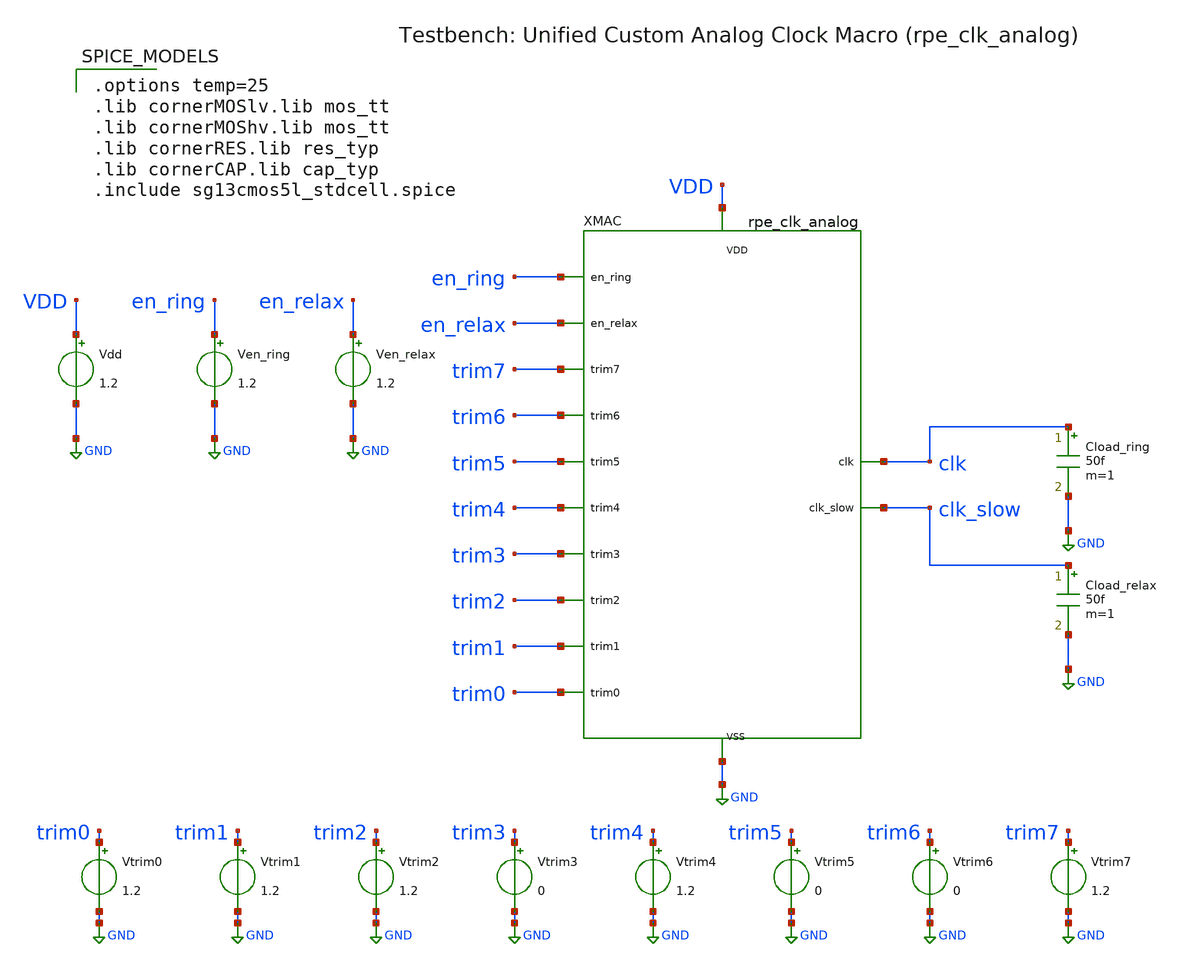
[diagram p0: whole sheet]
** sch_path: analog/clk_macro/tb_rpe_clk_analog.sch
**.subckt tb_rpe_clk_analog
XMAC VDD GND en_ring en_relax trim7 trim6 trim5 trim4 trim3 trim2 trim1 trim0 clk clk_slow
+ rpe_clk_analog
Vdd VDD GND 1.2
Ven_ring en_ring GND 1.2
Ven_relax en_relax GND 1.2
Vtrim0 trim0 GND 1.2
Vtrim1 trim1 GND 1.2
Vtrim2 trim2 GND 1.2
Vtrim3 trim3 GND 0
Vtrim4 trim4 GND 1.2
Vtrim5 trim5 GND 0
Vtrim6 trim6 GND 0
Vtrim7 trim7 GND 1.2
Cload_ring clk GND 50f m=1
Cload_relax clk_slow GND 50f m=1
**** begin user architecture code

.options temp=25
.lib cornerMOSlv.lib mos_tt
.lib cornerMOShv.lib mos_tt
.lib cornerRES.lib res_typ
.lib cornerCAP.lib cap_typ
.include sg13cmos5l_stdcell.spice


**** end user architecture code
**.ends

* expanding   symbol:  clk_macro/rpe_clk_analog.sym # of pins=14
** sym_path: analog/clk_macro/rpe_clk_analog.sym
** sch_path: analog/clk_macro/rpe_clk_analog.sch
.subckt rpe_clk_analog VDD VSS en_ring en_relax trim7 trim6 trim5 trim4 trim3 trim2 trim1 trim0 clk
+ clk_slow
*.iopin VDD
*.iopin VSS
*.ipin en_ring
*.ipin en_relax
*.ipin trim7
*.ipin trim6
*.ipin trim5
*.ipin trim4
*.ipin trim3
*.ipin trim2
*.ipin trim1
*.ipin trim0
*.opin clk
*.opin clk_slow
XEN_NOR net1 en_ring en_relax VDD VSS sg13cmos5l_nor2_1
XEN_OR en_bias net1 VDD VSS sg13cmos5l_inv_1
XBIAS VDD VSS en_bias vpbias vnbias net2 bias
* noconn #net2
XIDAC VDD VSS en_ring vnbias trim7 trim6 trim5 trim4 trim3 trim2 trim1 trim0 ictrl idac_8b
XCCO VDD VSS en_ring ictrl clk cco_core
XRELAX VDD VSS en_relax vpbias vnbias clk_slow relax_core
.ends


* expanding   symbol:  bias/bias.sym # of pins=6
** sym_path: analog/bias/bias.sym
** sch_path: analog/bias/bias.sch
.subckt bias VDD VSS en vpbias vnbias ibias_out
*.iopin VDD
*.iopin VSS
*.ipin en
*.opin vpbias
*.opin vnbias
*.opin ibias_out
XMEN_P enb en VDD VDD sg13_lv_pmos w=0.5u l=0.5u ng=1 m=1 mm_ok=1
XMEN_N enb en VSS VSS sg13_lv_nmos w=0.25u l=0.5u ng=1 m=1 mm_ok=1
XMSU_EN net1 enb VDD VDD sg13_lv_pmos w=0.3u l=1.0u ng=1 m=1 mm_ok=1
XMSU_P1 net2 VSS net1 VDD sg13_lv_pmos w=0.15u l=10u ng=1 m=1 mm_ok=1
XMSU_P2 net3 VSS net2 VDD sg13_lv_pmos w=0.15u l=10u ng=1 m=1 mm_ok=1
XMSU_N net3 vnbias VSS VSS sg13_lv_nmos w=4.0u l=0.5u ng=1 m=1 mm_ok=1
XMSU_INJ vpbias net3 VSS VSS sg13_lv_nmos w=0.5u l=1.0u ng=1 m=1 mm_ok=1
XMP1 vnbias vpbias VDD VDD sg13_lv_pmos w=1.0u l=4.0u ng=1 m=1 mm_ok=1
XMN1 vnbias vnbias VSS VSS sg13_lv_nmos w=0.3u l=4.0u ng=1 m=1 mm_ok=1
XMP2 vpbias vpbias VDD VDD sg13_lv_pmos w=1.0u l=4.0u ng=1 m=1 mm_ok=1
XMN2 vpbias vnbias net4 VSS sg13_lv_nmos w=0.3u l=4.0u ng=1 m=4 mm_ok=1
XR_BIAS net4 VSS VSS rppd w=0.5e-6 l=20.0e-6 m=1 b=19 mm_ok=1
XMP_OFF vpbias en VDD VDD sg13_lv_pmos w=1.0u l=0.5u ng=1 m=1 mm_ok=1
XMN_OFF vnbias enb VSS VSS sg13_lv_nmos w=1.0u l=0.5u ng=1 m=1 mm_ok=1
XMP_OUT ibias_out vpbias VDD VDD sg13_lv_pmos w=1.0u l=4.0u ng=1 m=1 mm_ok=1
.ends


* expanding   symbol:  osc_ring_cc/idac_8b.sym # of pins=13
** sym_path: analog/osc_ring_cc/idac_8b.sym
** sch_path: analog/osc_ring_cc/idac_8b.sch
.subckt idac_8b VDD VSS en vnbias trim7 trim6 trim5 trim4 trim3 trim2 trim1 trim0 ictrl
*.iopin VDD
*.iopin VSS
*.ipin en
*.ipin vnbias
*.ipin trim7
*.ipin trim6
*.ipin trim5
*.ipin trim4
*.ipin trim3
*.ipin trim2
*.ipin trim1
*.ipin trim0
*.opin ictrl
XMN_DIV vpdac vnbias VSS VSS sg13_lv_nmos w=0.3u l=4.0u ng=1 m=1 mm_ok=1
XMP_IN vpdac vpdac VDD VDD sg13_lv_pmos w=1.5u l=4.0u ng=1 m=2 mm_ok=1
XMP_DAC_OFF vpdac en VDD VDD sg13_lv_pmos w=0.5u l=0.5u ng=1 m=1 mm_ok=1
XINV_EN enb en VDD VSS sg13cmos5l_inv_1
XINV_B0 b0_b trim0 VDD VSS sg13cmos5l_inv_1
XINV_B1 b1_b trim1 VDD VSS sg13cmos5l_inv_1
XINV_B2 b2_b trim2 VDD VSS sg13cmos5l_inv_1
XINV_B3 b3_b trim3 VDD VSS sg13cmos5l_inv_1
XINV_B4 b4_b trim4 VDD VSS sg13cmos5l_inv_1
XINV_A t3_b trim7 VDD VSS sg13cmos5l_inv_1
XN_AB t5_b trim7 trim6 VDD VSS sg13cmos5l_nand2_2
XI_AB ab t5_b VDD VSS sg13cmos5l_inv_1
XN_ABC t6_b ab trim5 VDD VSS sg13cmos5l_nand2_2
XN_BC bc_n trim6 trim5 VDD VSS sg13cmos5l_nand2_2
XI_BC bc bc_n VDD VSS sg13cmos5l_inv_1
XNO_T2 t2_b trim7 bc VDD VSS sg13cmos5l_nor2_1
XNO_BORC borc_n trim6 trim5 VDD VSS sg13cmos5l_nor2_1
XI_BORC borc borc_n VDD VSS sg13cmos5l_inv_1
XN_T4 t4_b trim7 borc VDD VSS sg13cmos5l_nand2_2
XNO_T1 t1_b trim7 trim6 VDD VSS sg13cmos5l_nor2_1
XNO_T0 t0_b trim7 borc VDD VSS sg13cmos5l_nor2_1
XMPC_PED net1 vpdac VDD VDD sg13_lv_pmos w=0.5u l=4.0u ng=1 m=48 mm_ok=1
XMPS_PED ictrl enb net1 VDD sg13_lv_pmos w=1.0u l=0.2u ng=1 m=4 mm_ok=1
XMPC_B0 net2 vpdac VDD VDD sg13_lv_pmos w=0.5u l=4.0u ng=1 m=1 mm_ok=1
XMPS_B0 ictrl b0_b net2 VDD sg13_lv_pmos w=1.0u l=0.2u ng=1 m=1 mm_ok=1
XMPC_B1 net3 vpdac VDD VDD sg13_lv_pmos w=0.5u l=4.0u ng=1 m=2 mm_ok=1
XMPS_B1 ictrl b1_b net3 VDD sg13_lv_pmos w=1.0u l=0.2u ng=1 m=1 mm_ok=1
XMPC_B2 net4 vpdac VDD VDD sg13_lv_pmos w=0.5u l=4.0u ng=1 m=4 mm_ok=1
XMPS_B2 ictrl b2_b net4 VDD sg13_lv_pmos w=1.0u l=0.2u ng=1 m=1 mm_ok=1
XMPC_B3 net5 vpdac VDD VDD sg13_lv_pmos w=0.5u l=4.0u ng=1 m=8 mm_ok=1
XMPS_B3 ictrl b3_b net5 VDD sg13_lv_pmos w=1.0u l=0.2u ng=1 m=1 mm_ok=1
XMPC_B4 net6 vpdac VDD VDD sg13_lv_pmos w=0.5u l=4.0u ng=1 m=16 mm_ok=1
XMPS_B4 ictrl b4_b net6 VDD sg13_lv_pmos w=1.0u l=0.2u ng=1 m=2 mm_ok=1
XMPC_T0 net7 vpdac VDD VDD sg13_lv_pmos w=0.5u l=4.0u ng=1 m=32 mm_ok=1
XMPS_T0 ictrl t0_b net7 VDD sg13_lv_pmos w=1.0u l=0.2u ng=1 m=4 mm_ok=1
XMPC_T1 net8 vpdac VDD VDD sg13_lv_pmos w=0.5u l=4.0u ng=1 m=32 mm_ok=1
XMPS_T1 ictrl t1_b net8 VDD sg13_lv_pmos w=1.0u l=0.2u ng=1 m=4 mm_ok=1
XMPC_T2 net9 vpdac VDD VDD sg13_lv_pmos w=0.5u l=4.0u ng=1 m=32 mm_ok=1
XMPS_T2 ictrl t2_b net9 VDD sg13_lv_pmos w=1.0u l=0.2u ng=1 m=4 mm_ok=1
XMPC_T3 net10 vpdac VDD VDD sg13_lv_pmos w=0.5u l=4.0u ng=1 m=32 mm_ok=1
XMPS_T3 ictrl t3_b net10 VDD sg13_lv_pmos w=1.0u l=0.2u ng=1 m=4 mm_ok=1
XMPC_T4 net11 vpdac VDD VDD sg13_lv_pmos w=0.5u l=4.0u ng=1 m=32 mm_ok=1
XMPS_T4 ictrl t4_b net11 VDD sg13_lv_pmos w=1.0u l=0.2u ng=1 m=4 mm_ok=1
XMPC_T5 net12 vpdac VDD VDD sg13_lv_pmos w=0.5u l=4.0u ng=1 m=32 mm_ok=1
XMPS_T5 ictrl t5_b net12 VDD sg13_lv_pmos w=1.0u l=0.2u ng=1 m=4 mm_ok=1
XMPC_T6 net13 vpdac VDD VDD sg13_lv_pmos w=0.5u l=4.0u ng=1 m=32 mm_ok=1
XMPS_T6 ictrl t6_b net13 VDD sg13_lv_pmos w=1.0u l=0.2u ng=1 m=4 mm_ok=1
.ends


* expanding   symbol:  osc_ring_cc/cco_core.sym # of pins=5
** sym_path: analog/osc_ring_cc/cco_core.sym
** sch_path: analog/osc_ring_cc/cco_core.sch
.subckt cco_core VDD VSS en ictrl clk
*.iopin VDD
*.iopin VSS
*.ipin en
*.ipin ictrl
*.opin clk
XINV_EN enb en VDD VSS sg13cmos5l_inv_1
XMN_BIAS ictrl ictrl VSS VSS sg13_lv_nmos w=2.0u l=1.0u ng=1 m=2 mm_ok=1
XMP_BIAS vctrl_p vctrl_p VDD VDD sg13_lv_pmos w=4.0u l=1.0u ng=1 m=2 mm_ok=1
XMN_BMIR vctrl_p ictrl VSS VSS sg13_lv_nmos w=2.0u l=1.0u ng=1 m=2 mm_ok=1
XMP_POFF vctrl_p en VDD VDD sg13_lv_pmos w=0.5u l=0.5u ng=1 m=1 mm_ok=1
XMN_NOFF ictrl enb VSS VSS sg13_lv_nmos w=0.5u l=0.5u ng=1 m=1 mm_ok=1
XMPC_0 net1 vctrl_p VDD VDD sg13_lv_pmos w=4.0u l=1.0u ng=1 m=1 mm_ok=1
XMPI_0 n1 n0 net1 VDD sg13_lv_pmos w=1.0u l=0.2u ng=1 m=1 mm_ok=1
XMNI_0 n1 n0 net2 VSS sg13_lv_nmos w=0.5u l=0.2u ng=1 m=1 mm_ok=1
XMNC_0 net2 ictrl VSS VSS sg13_lv_nmos w=2.0u l=1.0u ng=1 m=1 mm_ok=1
XCC_0 n1 VSS cap_cmomf w=2.4e-6 l=2.4e-6 mmin=1 mmax=4 subblock=0 rfmodel=0 subscale=1 m=1 mm_ok=1
XMPC_1 net3 vctrl_p VDD VDD sg13_lv_pmos w=4.0u l=1.0u ng=1 m=1 mm_ok=1
XMPI_1 n2 n1 net3 VDD sg13_lv_pmos w=1.0u l=0.2u ng=1 m=1 mm_ok=1
XMNI_1 n2 n1 net4 VSS sg13_lv_nmos w=0.5u l=0.2u ng=1 m=1 mm_ok=1
XMNC_1 net4 ictrl VSS VSS sg13_lv_nmos w=2.0u l=1.0u ng=1 m=1 mm_ok=1
XCC_1 n2 VSS cap_cmomf w=2.4e-6 l=2.4e-6 mmin=1 mmax=4 subblock=0 rfmodel=0 subscale=1 m=1 mm_ok=1
XMPC_2 net5 vctrl_p VDD VDD sg13_lv_pmos w=4.0u l=1.0u ng=1 m=1 mm_ok=1
XMPI_2 n3 n2 net5 VDD sg13_lv_pmos w=1.0u l=0.2u ng=1 m=1 mm_ok=1
XMNI_2 n3 n2 net6 VSS sg13_lv_nmos w=0.5u l=0.2u ng=1 m=1 mm_ok=1
XMNC_2 net6 ictrl VSS VSS sg13_lv_nmos w=2.0u l=1.0u ng=1 m=1 mm_ok=1
XCC_2 n3 VSS cap_cmomf w=2.4e-6 l=2.4e-6 mmin=1 mmax=4 subblock=0 rfmodel=0 subscale=1 m=1 mm_ok=1
XMPC_3 net7 vctrl_p VDD VDD sg13_lv_pmos w=4.0u l=1.0u ng=1 m=1 mm_ok=1
XMPI_3 n4 n3 net7 VDD sg13_lv_pmos w=1.0u l=0.2u ng=1 m=1 mm_ok=1
XMNI_3 n4 n3 net8 VSS sg13_lv_nmos w=0.5u l=0.2u ng=1 m=1 mm_ok=1
XMNC_3 net8 ictrl VSS VSS sg13_lv_nmos w=2.0u l=1.0u ng=1 m=1 mm_ok=1
XCC_3 n4 VSS cap_cmomf w=2.4e-6 l=2.4e-6 mmin=1 mmax=4 subblock=0 rfmodel=0 subscale=1 m=1 mm_ok=1
XMPC_4 net9 vctrl_p VDD VDD sg13_lv_pmos w=4.0u l=1.0u ng=1 m=1 mm_ok=1
XMPI_4 n0 n4 net9 VDD sg13_lv_pmos w=1.0u l=0.2u ng=1 m=1 mm_ok=1
XMNI_4 n0 n4 net10 VSS sg13_lv_nmos w=0.5u l=0.2u ng=1 m=1 mm_ok=1
XMNC_4 net10 ictrl VSS VSS sg13_lv_nmos w=2.0u l=1.0u ng=1 m=1 mm_ok=1
XCC_4 n0 VSS cap_cmomf w=2.4e-6 l=2.4e-6 mmin=1 mmax=4 subblock=0 rfmodel=0 subscale=1 m=1 mm_ok=1
XMN_RST n4 enb VSS VSS sg13_lv_nmos w=0.5u l=0.5u ng=1 m=1 mm_ok=1
XBUF1 net11 n4 VDD VSS sg13cmos5l_inv_1
XBUF2 net12 net11 VDD VSS sg13cmos5l_inv_2
XBUF4 clk net12 VDD VSS sg13cmos5l_buf_4
.ends


* expanding   symbol:  clk_macro/relax_core.sym # of pins=6
** sym_path: analog/clk_macro/relax_core.sym
** sch_path: analog/clk_macro/relax_core.sch
.subckt relax_core VDD VSS en vpbias vnbias clk_slow
*.iopin VDD
*.iopin VSS
*.ipin en
*.ipin vpbias
*.ipin vnbias
*.opin clk_slow
XINV_EN enb en VDD VSS sg13cmos5l_inv_1
XMP_REF vth vpbias VDD VDD sg13_lv_pmos w=1.0u l=4.0u ng=1 m=1 mm_ok=1
XR_TH0 vth net1 VSS rppd w=0.5e-6 l=40.0e-6 m=1 b=9 mm_ok=1
XR_TH1 net1 net2 VSS rppd w=0.5e-6 l=40.0e-6 m=1 b=9 mm_ok=1
XR_TH2 net2 net3 VSS rppd w=0.5e-6 l=40.0e-6 m=1 b=9 mm_ok=1
XR_TH3 net3 VSS VSS rppd w=0.5e-6 l=40.0e-6 m=1 b=9 mm_ok=1
XMN_MIR vp_chg vnbias VSS VSS sg13_lv_nmos w=0.3u l=4.0u ng=1 m=1 mm_ok=1
XMP_CHG_IN vp_chg vp_chg VDD VDD sg13_lv_pmos w=0.5u l=4.0u ng=1 m=10 mm_ok=1
XMP_CHG_A vcap_a vp_chg VDD VDD sg13_lv_pmos w=0.5u l=4.0u ng=1 m=1 mm_ok=1
XMN_DIS_A vcap_a dis_a VSS VSS sg13_hv_nmos w=0.5u l=0.5u ng=1 m=1 mm_ok=1
XC_A vcap_a VSS vcap_a VSS sg13_hv_svaricap w=9.74e-6 l=0.8e-6 Nx=8 mm_ok=1
XCOMP_A VDD VSS en vpbias vcap_a vth cmp_a comp
XMP_CHG_B vcap_b vp_chg VDD VDD sg13_lv_pmos w=0.5u l=4.0u ng=1 m=1 mm_ok=1
XMN_DIS_B vcap_b dis_b VSS VSS sg13_hv_nmos w=0.5u l=0.5u ng=1 m=1 mm_ok=1
XC_B vcap_b VSS vcap_b VSS sg13_hv_svaricap w=9.74e-6 l=0.8e-6 Nx=8 mm_ok=1
XCOMP_B VDD VSS en vpbias vcap_b vth cmp_b comp
XSR_Q q cmp_b qb VDD VSS sg13cmos5l_nor2_1
XSR_QB qb cmp_a q VDD VSS sg13cmos5l_nor2_1
XMN_INIT qb enb VSS VSS sg13_lv_nmos w=0.5u l=0.5u ng=1 m=1 mm_ok=1
XDIS_N_A net4 q enb VDD VSS sg13cmos5l_nor2_1
XDIS_I_A dis_a net4 VDD VSS sg13cmos5l_inv_1
XDIS_N_B net5 qb enb VDD VSS sg13cmos5l_nor2_1
XDIS_I_B dis_b net5 VDD VSS sg13cmos5l_inv_1
XBOTH_NAND net6 cmp_a cmp_b VDD VSS sg13cmos5l_nand2_2
XBOTH_INV net7 net6 VDD VSS sg13cmos5l_inv_1
XMN_UNSTICK vcap_a net7 VSS VSS sg13_hv_nmos w=0.5u l=0.5u ng=1 m=1 mm_ok=1
XOUT_NOR net8 qb enb VDD VSS sg13cmos5l_nor2_1
XOUT_BUF clk_slow net8 VDD VSS sg13cmos5l_buf_2
.ends


* expanding   symbol:  osc_relax/comp.sym # of pins=7
** sym_path: analog/osc_relax/comp.sym
** sch_path: analog/osc_relax/comp.sch
.subckt comp VDD VSS en vpbias inp inn out
*.iopin VDD
*.iopin VSS
*.ipin en
*.ipin vpbias
*.ipin inp
*.ipin inn
*.opin out
XMP_TAIL net1 vpbias VDD VDD sg13_lv_pmos w=1.0u l=4.0u ng=1 m=1 mm_ok=1
XMP_INP net2 inp net1 VDD sg13_lv_pmos w=2.0u l=1.0u ng=1 m=2 mm_ok=1
XMP_INN net3 inn net1 VDD sg13_lv_pmos w=2.0u l=1.0u ng=1 m=2 mm_ok=1
XMN_L1 net2 net2 VSS VSS sg13_lv_nmos w=0.5u l=2.0u ng=1 m=1 mm_ok=1
XMN_L2 net3 net2 VSS VSS sg13_lv_nmos w=0.5u l=2.0u ng=1 m=1 mm_ok=1
XMP_G2 net4 vpbias VDD VDD sg13_lv_pmos w=1.0u l=4.0u ng=1 m=1 mm_ok=1
XMN_G2 net4 net3 VSS VSS sg13_lv_nmos w=1.0u l=1.0u ng=1 m=1 mm_ok=1
XMP_OFF net4 en VDD VDD sg13_lv_pmos w=0.5u l=0.5u ng=1 m=1 mm_ok=1
XINV_OUT out net4 VDD VSS sg13cmos5l_inv_1
.ends

.GLOBAL GND
.end
